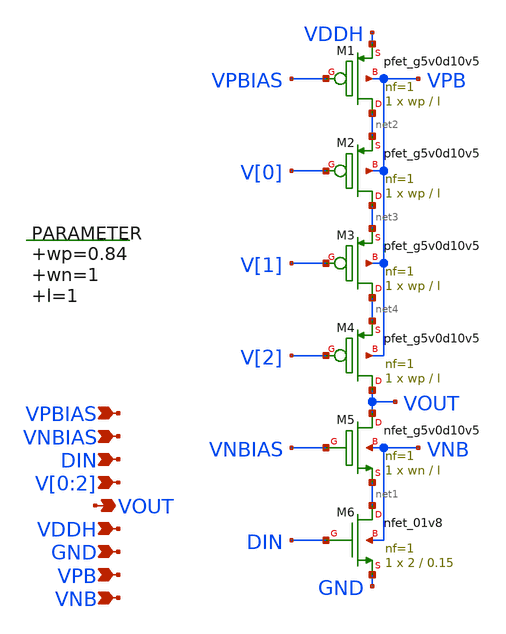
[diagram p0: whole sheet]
** sch_path: xschem/pull_up_down_network.sch
**.subckt pull_up_down_network VPBIAS VNBIAS DIN V[0],V[1],V[2] VOUT VDDH GND VPB VNB
*.ipin VPBIAS
*.ipin VNBIAS
*.ipin DIN
*.ipin V[0],V[1],V[2]
*.opin VOUT
*.ipin VDDH
*.ipin GND
*.ipin VPB
*.ipin VNB
XM1 net2 VPBIAS VDDH VPB sky130_fd_pr__pfet_g5v0d10v5 L=l W=wp nf=1 ad='int((nf+1)/2) * W/nf * 0.29'
+ as='int((nf+2)/2) * W/nf * 0.29' pd='2*int((nf+1)/2) * (W/nf + 0.29)' ps='2*int((nf+2)/2) * (W/nf + 0.29)'
+ nrd='0.29 / W' nrs='0.29 / W' sa=0 sb=0 sd=0 mult=1 m=1
.param wp=0.84 wn=1 l=1

XM2 net3 V[0] net2 VPB sky130_fd_pr__pfet_g5v0d10v5 L=l W=wp nf=1 ad='int((nf+1)/2) * W/nf * 0.29' as='int((nf+2)/2) * W/nf * 0.29'
+ pd='2*int((nf+1)/2) * (W/nf + 0.29)' ps='2*int((nf+2)/2) * (W/nf + 0.29)' nrd='0.29 / W' nrs='0.29 / W'
+ sa=0 sb=0 sd=0 mult=1 m=1
XM3 net4 V[1] net3 VPB sky130_fd_pr__pfet_g5v0d10v5 L=l W=wp nf=1 ad='int((nf+1)/2) * W/nf * 0.29' as='int((nf+2)/2) * W/nf * 0.29'
+ pd='2*int((nf+1)/2) * (W/nf + 0.29)' ps='2*int((nf+2)/2) * (W/nf + 0.29)' nrd='0.29 / W' nrs='0.29 / W'
+ sa=0 sb=0 sd=0 mult=1 m=1
XM4 VOUT V[2] net4 VPB sky130_fd_pr__pfet_g5v0d10v5 L=l W=wp nf=1 ad='int((nf+1)/2) * W/nf * 0.29' as='int((nf+2)/2) * W/nf * 0.29'
+ pd='2*int((nf+1)/2) * (W/nf + 0.29)' ps='2*int((nf+2)/2) * (W/nf + 0.29)' nrd='0.29 / W' nrs='0.29 / W'
+ sa=0 sb=0 sd=0 mult=1 m=1
XM5 VOUT VNBIAS net1 VNB sky130_fd_pr__nfet_g5v0d10v5 L=l W=wn nf=1 ad='int((nf+1)/2) * W/nf * 0.29'
+ as='int((nf+2)/2) * W/nf * 0.29' pd='2*int((nf+1)/2) * (W/nf + 0.29)' ps='2*int((nf+2)/2) * (W/nf + 0.29)'
+ nrd='0.29 / W' nrs='0.29 / W' sa=0 sb=0 sd=0 mult=1 m=1
XM6 net1 DIN GND VNB sky130_fd_pr__nfet_01v8 L=0.15 W=2 nf=1 ad='int((nf+1)/2) * W/nf * 0.29' as='int((nf+2)/2) * W/nf * 0.29'
+ pd='2*int((nf+1)/2) * (W/nf + 0.29)' ps='2*int((nf+2)/2) * (W/nf + 0.29)' nrd='0.29 / W' nrs='0.29 / W'
+ sa=0 sb=0 sd=0 mult=1 m=1
**.ends
.end
